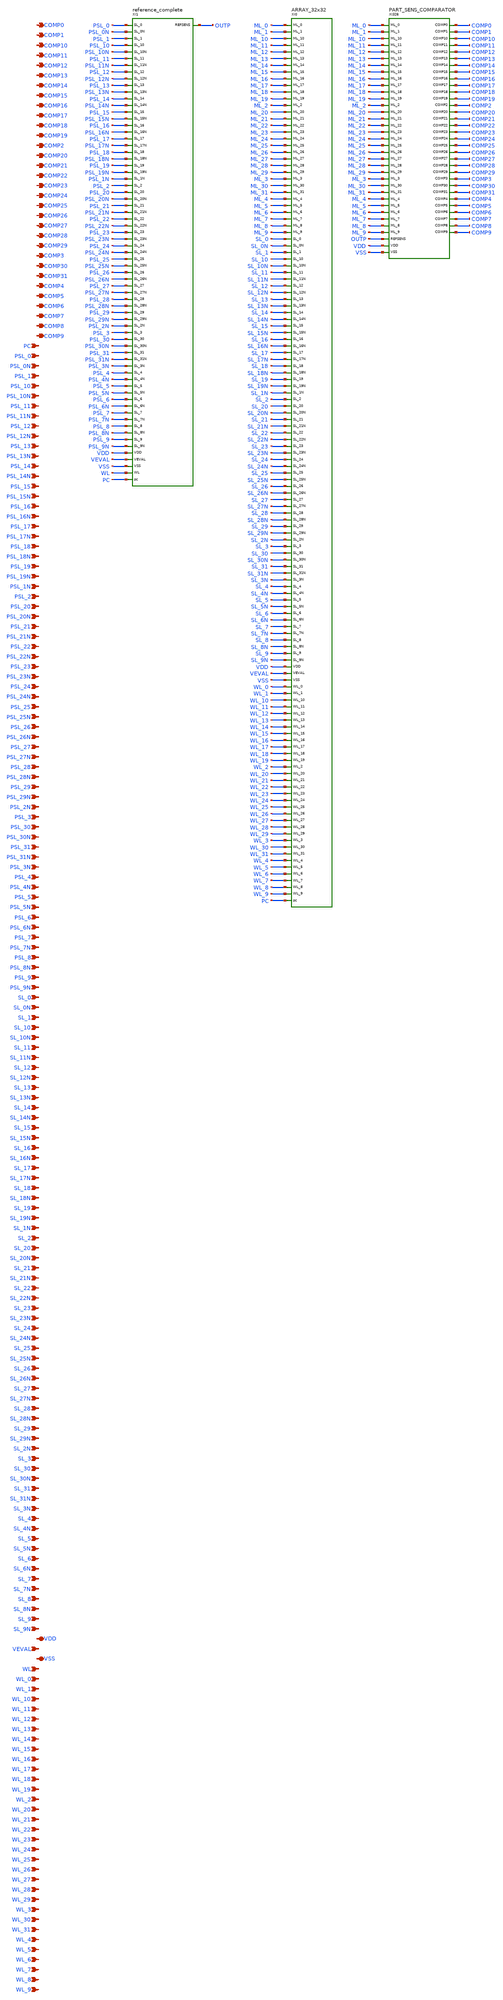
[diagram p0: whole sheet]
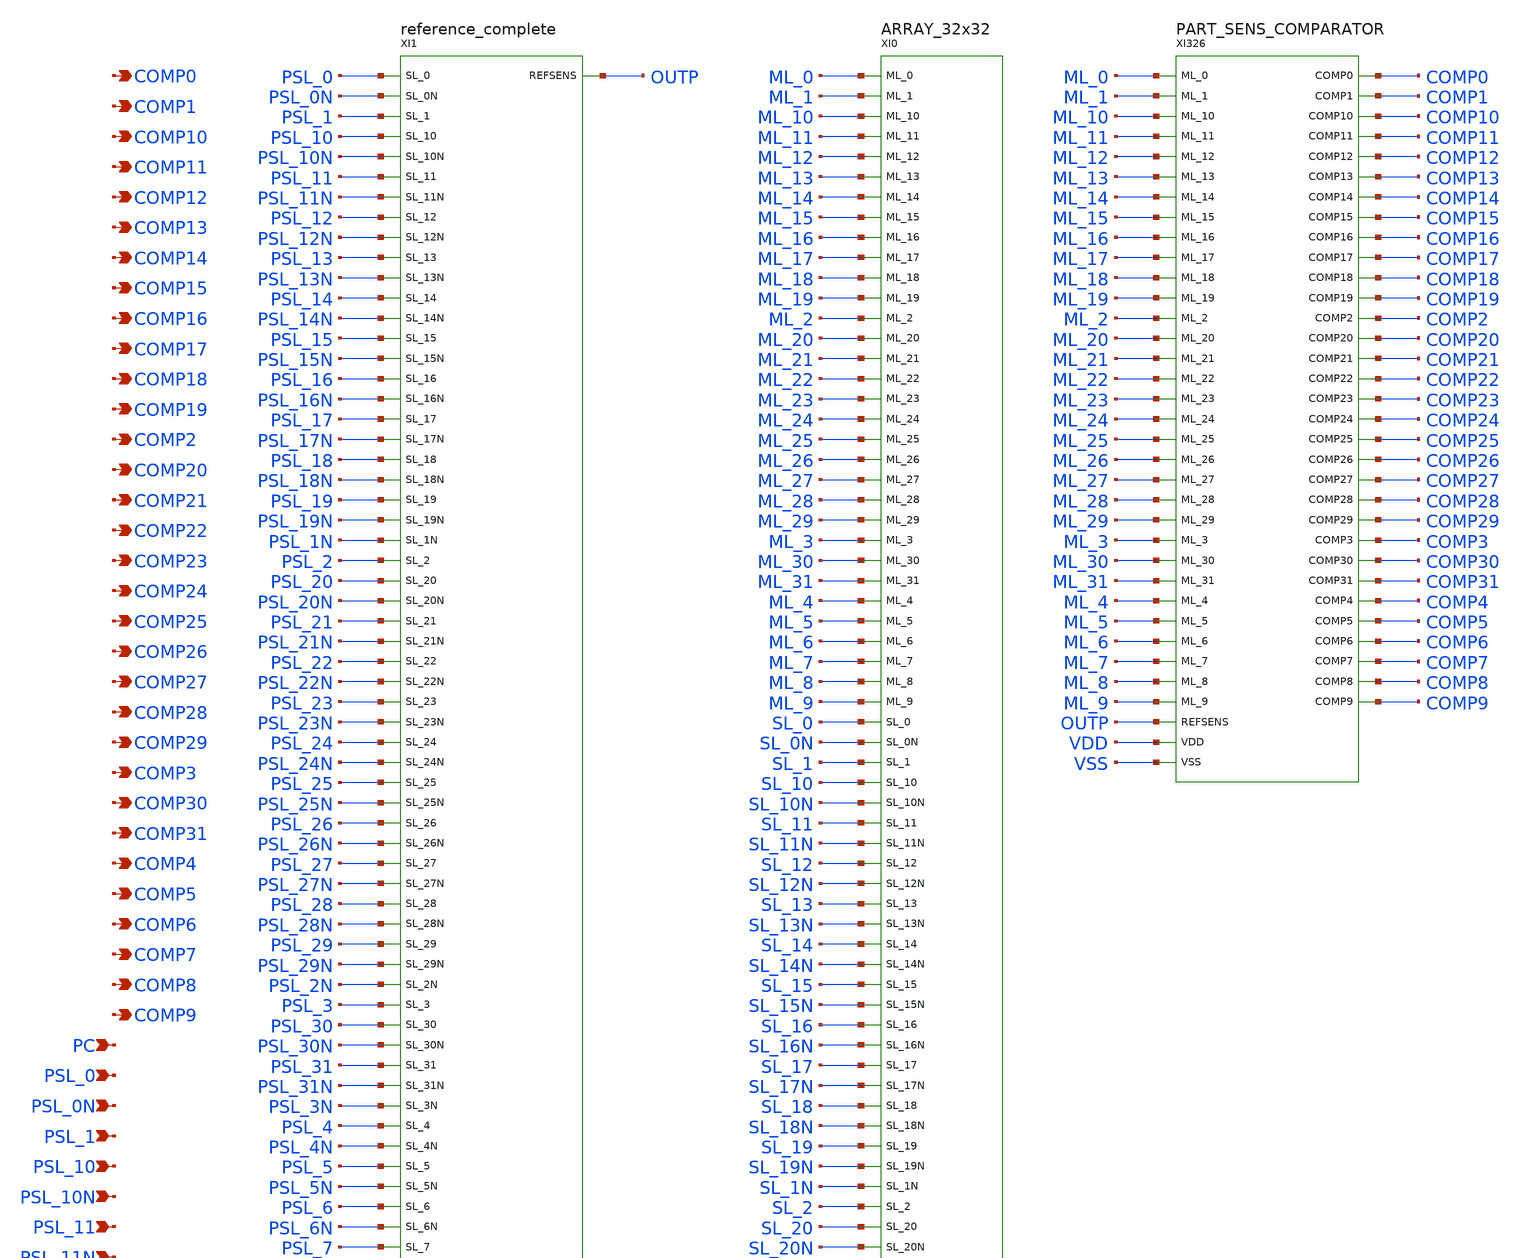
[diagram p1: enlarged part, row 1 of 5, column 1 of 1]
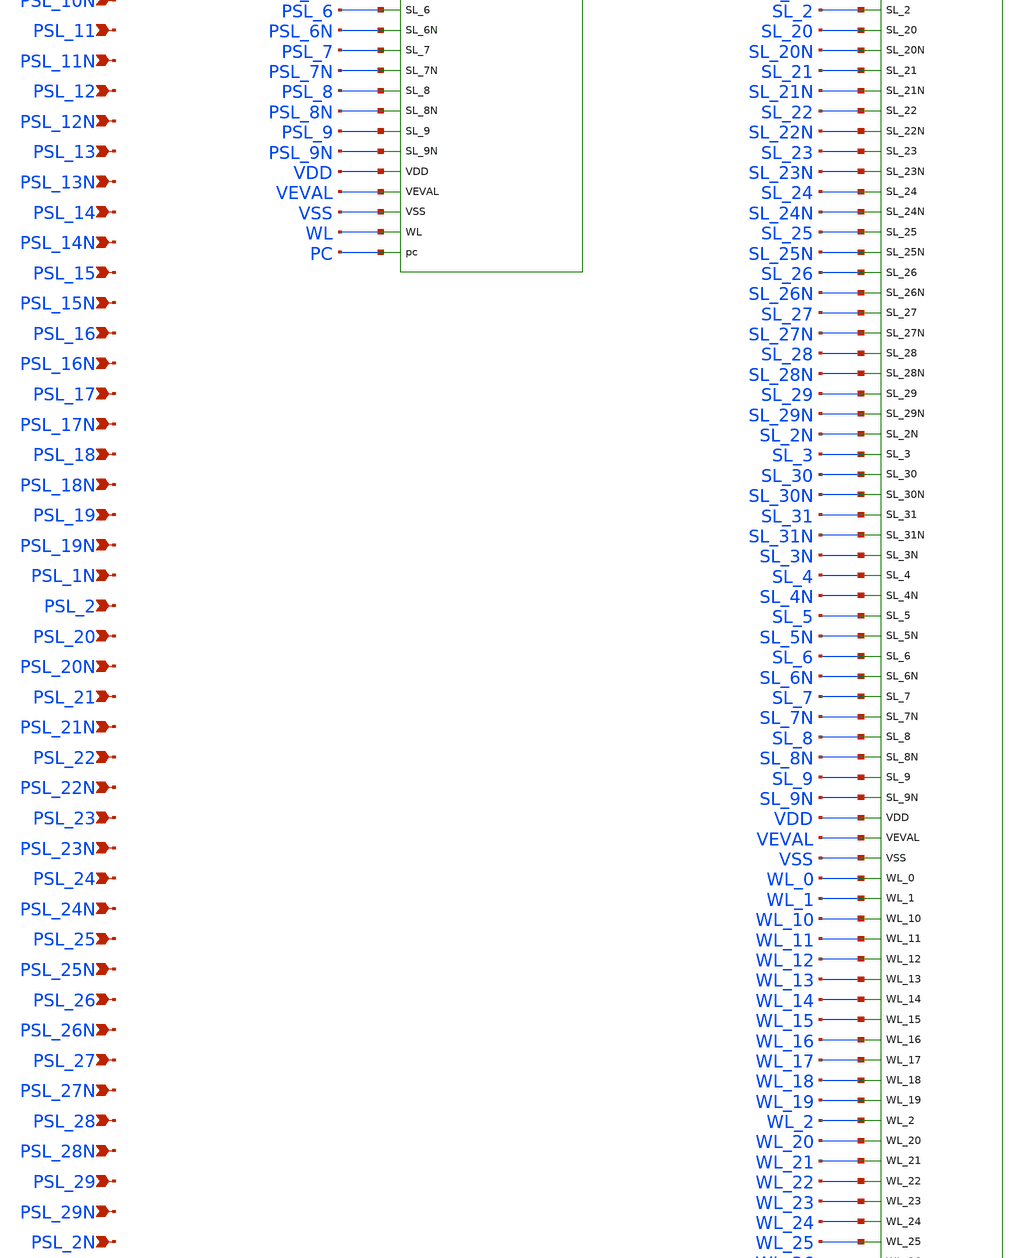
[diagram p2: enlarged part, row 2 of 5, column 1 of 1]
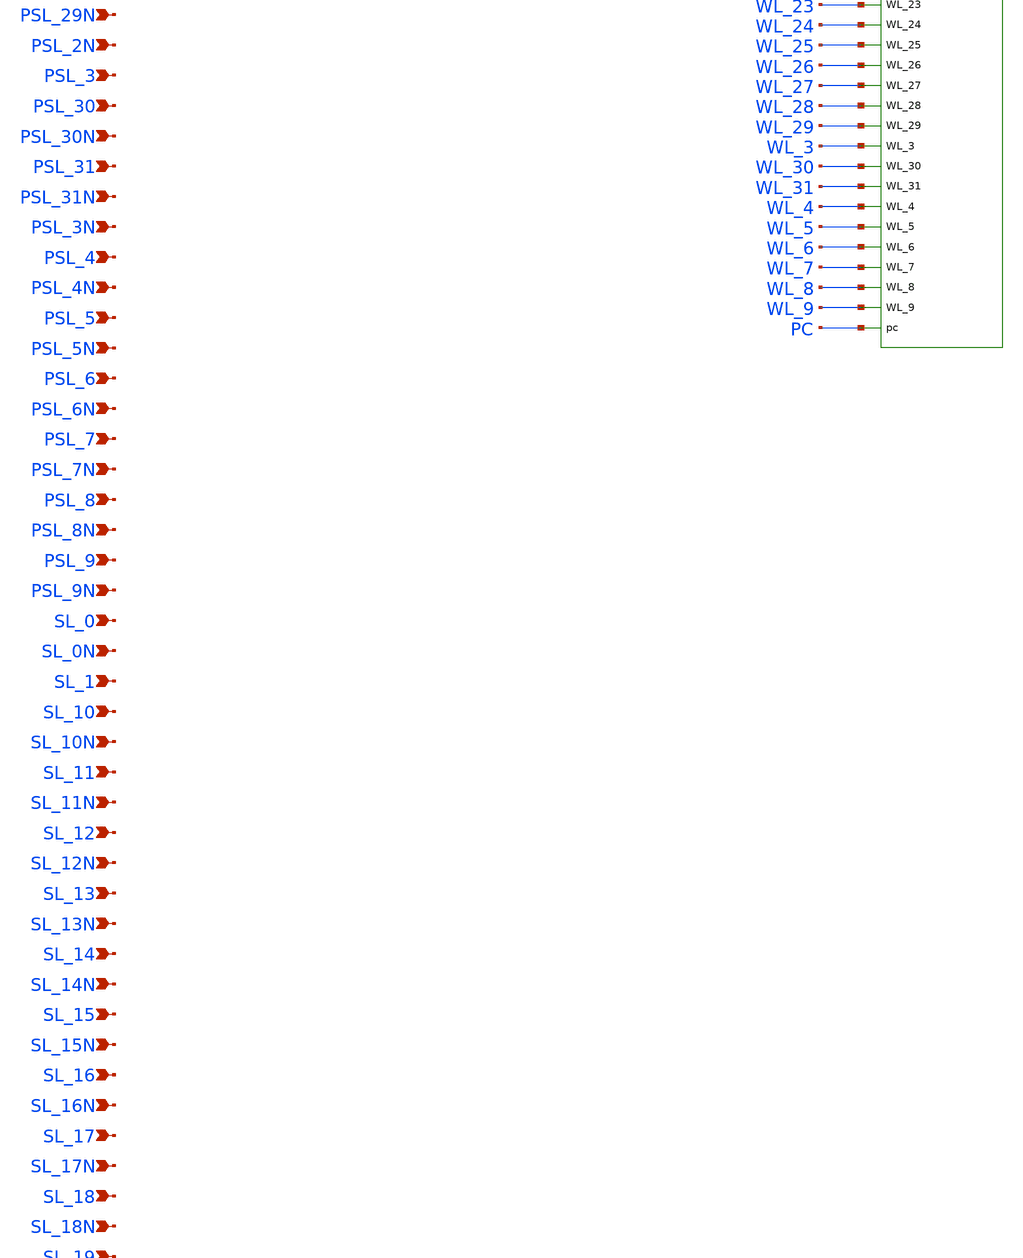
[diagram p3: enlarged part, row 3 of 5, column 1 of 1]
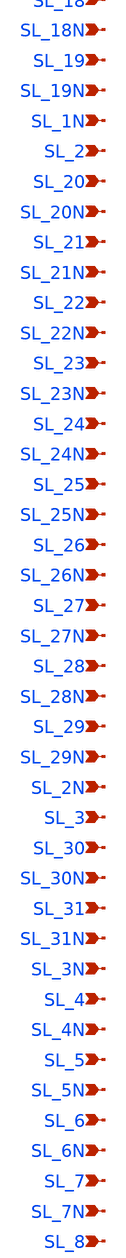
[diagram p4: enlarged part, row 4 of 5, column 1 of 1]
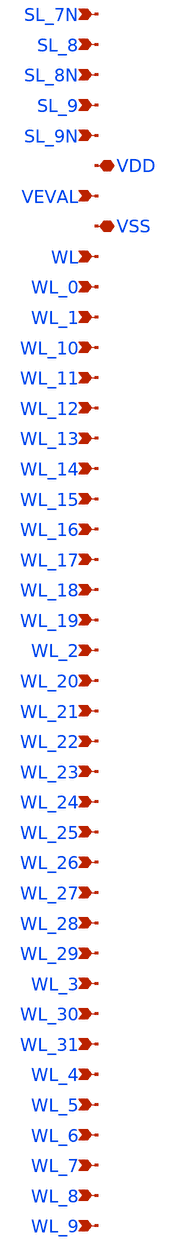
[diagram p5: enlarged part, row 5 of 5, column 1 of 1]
** sch_path: SoC6169-main/schematic/xschem/ANALOG_FIGURE.sch
* Copyright 2026 USFQ CAM team
* Licensed under the Apache License, Version 2.0 (the "License");
* you may not use this file except in compliance with the License.
* You may obtain a copy of the License at
* https://www.apache.org/licenses/LICENSE-2.0
* Unless required by applicable law or agreed to in writing, software
* distributed under the License is distributed on an "AS IS" BASIS,
* WITHOUT WARRANTIES OR CONDITIONS OF ANY KIND, either express or implied.
* See the License for the specific language governing permissions and
* limitations under the License.
**.subckt ANALOG_FIGURE COMP0 COMP1 COMP10 COMP11 COMP12 COMP13 COMP14 COMP15 COMP16 COMP17 COMP18
*+ COMP19 COMP2 COMP20 COMP21 COMP22 COMP23 COMP24 COMP25 COMP26 COMP27 COMP28 COMP29 COMP3 COMP30 COMP31
*+ COMP4 COMP5 COMP6 COMP7 COMP8 COMP9 PC PSL_0 PSL_0N PSL_1 PSL_10 PSL_10N PSL_11 PSL_11N PSL_12 PSL_12N
*+ PSL_13 PSL_13N PSL_14 PSL_14N PSL_15 PSL_15N PSL_16 PSL_16N PSL_17 PSL_17N PSL_18 PSL_18N PSL_19 PSL_19N
*+ PSL_1N PSL_2 PSL_20 PSL_20N PSL_21 PSL_21N PSL_22 PSL_22N PSL_23 PSL_23N PSL_24 PSL_24N PSL_25 PSL_25N
*+ PSL_26 PSL_26N PSL_27 PSL_27N PSL_28 PSL_28N PSL_29 PSL_29N PSL_2N PSL_3 PSL_30 PSL_30N PSL_31 PSL_31N
*+ PSL_3N PSL_4 PSL_4N PSL_5 PSL_5N PSL_6 PSL_6N PSL_7 PSL_7N PSL_8 PSL_8N PSL_9 PSL_9N SL_0 SL_0N SL_1 SL_10
*+ SL_10N SL_11 SL_11N SL_12 SL_12N SL_13 SL_13N SL_14 SL_14N SL_15 SL_15N SL_16 SL_16N SL_17 SL_17N SL_18
*+ SL_18N SL_19 SL_19N SL_1N SL_2 SL_20 SL_20N SL_21 SL_21N SL_22 SL_22N SL_23 SL_23N SL_24 SL_24N SL_25
*+ SL_25N SL_26 SL_26N SL_27 SL_27N SL_28 SL_28N SL_29 SL_29N SL_2N SL_3 SL_30 SL_30N SL_31 SL_31N SL_3N SL_4
*+ SL_4N SL_5 SL_5N SL_6 SL_6N SL_7 SL_7N SL_8 SL_8N SL_9 SL_9N VDD VEVAL VSS WL WL_0 WL_1 WL_10 WL_11 WL_12
*+ WL_13 WL_14 WL_15 WL_16 WL_17 WL_18 WL_19 WL_2 WL_20 WL_21 WL_22 WL_23 WL_24 WL_25 WL_26 WL_27 WL_28
*+ WL_29 WL_3 WL_30 WL_31 WL_4 WL_5 WL_6 WL_7 WL_8 WL_9
*.opin COMP0
*.opin COMP1
*.opin COMP10
*.opin COMP11
*.opin COMP12
*.opin COMP13
*.opin COMP14
*.opin COMP15
*.opin COMP16
*.opin COMP17
*.opin COMP18
*.opin COMP19
*.opin COMP2
*.opin COMP20
*.opin COMP21
*.opin COMP22
*.opin COMP23
*.opin COMP24
*.opin COMP25
*.opin COMP26
*.opin COMP27
*.opin COMP28
*.opin COMP29
*.opin COMP3
*.opin COMP30
*.opin COMP31
*.opin COMP4
*.opin COMP5
*.opin COMP6
*.opin COMP7
*.opin COMP8
*.opin COMP9
*.ipin PC
*.ipin PSL_0
*.ipin PSL_0N
*.ipin PSL_1
*.ipin PSL_10
*.ipin PSL_10N
*.ipin PSL_11
*.ipin PSL_11N
*.ipin PSL_12
*.ipin PSL_12N
*.ipin PSL_13
*.ipin PSL_13N
*.ipin PSL_14
*.ipin PSL_14N
*.ipin PSL_15
*.ipin PSL_15N
*.ipin PSL_16
*.ipin PSL_16N
*.ipin PSL_17
*.ipin PSL_17N
*.ipin PSL_18
*.ipin PSL_18N
*.ipin PSL_19
*.ipin PSL_19N
*.ipin PSL_1N
*.ipin PSL_2
*.ipin PSL_20
*.ipin PSL_20N
*.ipin PSL_21
*.ipin PSL_21N
*.ipin PSL_22
*.ipin PSL_22N
*.ipin PSL_23
*.ipin PSL_23N
*.ipin PSL_24
*.ipin PSL_24N
*.ipin PSL_25
*.ipin PSL_25N
*.ipin PSL_26
*.ipin PSL_26N
*.ipin PSL_27
*.ipin PSL_27N
*.ipin PSL_28
*.ipin PSL_28N
*.ipin PSL_29
*.ipin PSL_29N
*.ipin PSL_2N
*.ipin PSL_3
*.ipin PSL_30
*.ipin PSL_30N
*.ipin PSL_31
*.ipin PSL_31N
*.ipin PSL_3N
*.ipin PSL_4
*.ipin PSL_4N
*.ipin PSL_5
*.ipin PSL_5N
*.ipin PSL_6
*.ipin PSL_6N
*.ipin PSL_7
*.ipin PSL_7N
*.ipin PSL_8
*.ipin PSL_8N
*.ipin PSL_9
*.ipin PSL_9N
*.ipin SL_0
*.ipin SL_0N
*.ipin SL_1
*.ipin SL_10
*.ipin SL_10N
*.ipin SL_11
*.ipin SL_11N
*.ipin SL_12
*.ipin SL_12N
*.ipin SL_13
*.ipin SL_13N
*.ipin SL_14
*.ipin SL_14N
*.ipin SL_15
*.ipin SL_15N
*.ipin SL_16
*.ipin SL_16N
*.ipin SL_17
*.ipin SL_17N
*.ipin SL_18
*.ipin SL_18N
*.ipin SL_19
*.ipin SL_19N
*.ipin SL_1N
*.ipin SL_2
*.ipin SL_20
*.ipin SL_20N
*.ipin SL_21
*.ipin SL_21N
*.ipin SL_22
*.ipin SL_22N
*.ipin SL_23
*.ipin SL_23N
*.ipin SL_24
*.ipin SL_24N
*.ipin SL_25
*.ipin SL_25N
*.ipin SL_26
*.ipin SL_26N
*.ipin SL_27
*.ipin SL_27N
*.ipin SL_28
*.ipin SL_28N
*.ipin SL_29
*.ipin SL_29N
*.ipin SL_2N
*.ipin SL_3
*.ipin SL_30
*.ipin SL_30N
*.ipin SL_31
*.ipin SL_31N
*.ipin SL_3N
*.ipin SL_4
*.ipin SL_4N
*.ipin SL_5
*.ipin SL_5N
*.ipin SL_6
*.ipin SL_6N
*.ipin SL_7
*.ipin SL_7N
*.ipin SL_8
*.ipin SL_8N
*.ipin SL_9
*.ipin SL_9N
*.iopin VDD
*.ipin VEVAL
*.iopin VSS
*.ipin WL
*.ipin WL_0
*.ipin WL_1
*.ipin WL_10
*.ipin WL_11
*.ipin WL_12
*.ipin WL_13
*.ipin WL_14
*.ipin WL_15
*.ipin WL_16
*.ipin WL_17
*.ipin WL_18
*.ipin WL_19
*.ipin WL_2
*.ipin WL_20
*.ipin WL_21
*.ipin WL_22
*.ipin WL_23
*.ipin WL_24
*.ipin WL_25
*.ipin WL_26
*.ipin WL_27
*.ipin WL_28
*.ipin WL_29
*.ipin WL_3
*.ipin WL_30
*.ipin WL_31
*.ipin WL_4
*.ipin WL_5
*.ipin WL_6
*.ipin WL_7
*.ipin WL_8
*.ipin WL_9
XI1 OUTP PSL_0 PSL_0N PSL_1 PSL_10 PSL_10N PSL_11 PSL_11N PSL_12 PSL_12N PSL_13 PSL_13N PSL_14
+ PSL_14N PSL_15 PSL_15N PSL_16 PSL_16N PSL_17 PSL_17N PSL_18 PSL_18N PSL_19 PSL_19N PSL_1N PSL_2 PSL_20
+ PSL_20N PSL_21 PSL_21N PSL_22 PSL_22N PSL_23 PSL_23N PSL_24 PSL_24N PSL_25 PSL_25N PSL_26 PSL_26N PSL_27
+ PSL_27N PSL_28 PSL_28N PSL_29 PSL_29N PSL_2N PSL_3 PSL_30 PSL_30N PSL_31 PSL_31N PSL_3N PSL_4 PSL_4N PSL_5
+ PSL_5N PSL_6 PSL_6N PSL_7 PSL_7N PSL_8 PSL_8N PSL_9 PSL_9N VDD VEVAL VSS WL PC reference_complete
XI0 ML_0 ML_1 ML_10 ML_11 ML_12 ML_13 ML_14 ML_15 ML_16 ML_17 ML_18 ML_19 ML_2 ML_20 ML_21 ML_22
+ ML_23 ML_24 ML_25 ML_26 ML_27 ML_28 ML_29 ML_3 ML_30 ML_31 ML_4 ML_5 ML_6 ML_7 ML_8 ML_9 SL_0 SL_0N SL_1
+ SL_10 SL_10N SL_11 SL_11N SL_12 SL_12N SL_13 SL_13N SL_14 SL_14N SL_15 SL_15N SL_16 SL_16N SL_17 SL_17N
+ SL_18 SL_18N SL_19 SL_19N SL_1N SL_2 SL_20 SL_20N SL_21 SL_21N SL_22 SL_22N SL_23 SL_23N SL_24 SL_24N
+ SL_25 SL_25N SL_26 SL_26N SL_27 SL_27N SL_28 SL_28N SL_29 SL_29N SL_2N SL_3 SL_30 SL_30N SL_31 SL_31N
+ SL_3N SL_4 SL_4N SL_5 SL_5N SL_6 SL_6N SL_7 SL_7N SL_8 SL_8N SL_9 SL_9N VDD VEVAL VSS WL_0 WL_1 WL_10
+ WL_11 WL_12 WL_13 WL_14 WL_15 WL_16 WL_17 WL_18 WL_19 WL_2 WL_20 WL_21 WL_22 WL_23 WL_24 WL_25 WL_26
+ WL_27 WL_28 WL_29 WL_3 WL_30 WL_31 WL_4 WL_5 WL_6 WL_7 WL_8 WL_9 PC ARRAY_32x32
XI326 COMP0 COMP1 COMP10 COMP11 COMP12 COMP13 COMP14 COMP15 COMP16 COMP17 COMP18 COMP19 COMP2 COMP20
+ COMP21 COMP22 COMP23 COMP24 COMP25 COMP26 COMP27 COMP28 COMP29 COMP3 COMP30 COMP31 COMP4 COMP5 COMP6 COMP7
+ COMP8 COMP9 ML_0 ML_1 ML_10 ML_11 ML_12 ML_13 ML_14 ML_15 ML_16 ML_17 ML_18 ML_19 ML_2 ML_20 ML_21 ML_22
+ ML_23 ML_24 ML_25 ML_26 ML_27 ML_28 ML_29 ML_3 ML_30 ML_31 ML_4 ML_5 ML_6 ML_7 ML_8 ML_9 OUTP VDD VSS
+ PART_SENS_COMPARATOR
**.ends

* expanding   symbol:  reference_complete.sym # of pins=70
** sym_path: SoC6169-main/schematic/xschem/reference_complete.sym
** sch_path: SoC6169-main/schematic/xschem/reference_complete.sch
.subckt reference_complete REFSENS SL_0 SL_0N SL_1 SL_10 SL_10N SL_11 SL_11N SL_12 SL_12N SL_13
+ SL_13N SL_14 SL_14N SL_15 SL_15N SL_16 SL_16N SL_17 SL_17N SL_18 SL_18N SL_19 SL_19N SL_1N SL_2 SL_20
+ SL_20N SL_21 SL_21N SL_22 SL_22N SL_23 SL_23N SL_24 SL_24N SL_25 SL_25N SL_26 SL_26N SL_27 SL_27N SL_28
+ SL_28N SL_29 SL_29N SL_2N SL_3 SL_30 SL_30N SL_31 SL_31N SL_3N SL_4 SL_4N SL_5 SL_5N SL_6 SL_6N SL_7 SL_7N
+ SL_8 SL_8N SL_9 SL_9N VDD VEVAL VSS WL pc
*.opin REFSENS
*.ipin SL_0
*.ipin SL_0N
*.ipin SL_1
*.ipin SL_10
*.ipin SL_10N
*.ipin SL_11
*.ipin SL_11N
*.ipin SL_12
*.ipin SL_12N
*.ipin SL_13
*.ipin SL_13N
*.ipin SL_14
*.ipin SL_14N
*.ipin SL_15
*.ipin SL_15N
*.ipin SL_16
*.ipin SL_16N
*.ipin SL_17
*.ipin SL_17N
*.ipin SL_18
*.ipin SL_18N
*.ipin SL_19
*.ipin SL_19N
*.ipin SL_1N
*.ipin SL_2
*.ipin SL_20
*.ipin SL_20N
*.ipin SL_21
*.ipin SL_21N
*.ipin SL_22
*.ipin SL_22N
*.ipin SL_23
*.ipin SL_23N
*.ipin SL_24
*.ipin SL_24N
*.ipin SL_25
*.ipin SL_25N
*.ipin SL_26
*.ipin SL_26N
*.ipin SL_27
*.ipin SL_27N
*.ipin SL_28
*.ipin SL_28N
*.ipin SL_29
*.ipin SL_29N
*.ipin SL_2N
*.ipin SL_3
*.ipin SL_30
*.ipin SL_30N
*.ipin SL_31
*.ipin SL_31N
*.ipin SL_3N
*.ipin SL_4
*.ipin SL_4N
*.ipin SL_5
*.ipin SL_5N
*.ipin SL_6
*.ipin SL_6N
*.ipin SL_7
*.ipin SL_7N
*.ipin SL_8
*.ipin SL_8N
*.ipin SL_9
*.ipin SL_9N
*.iopin VDD
*.ipin VEVAL
*.iopin VSS
*.ipin WL
*.ipin pc
XI311 REFSENS net1 VDD VSS BUFFER
XI323 VSS ML_ref VDD net1 INV
XI0 ML_ref SL_0 SL_0N SL_1 SL_10 SL_10N SL_11 SL_11N SL_12 SL_12N SL_13 SL_13N SL_14 SL_14N SL_15
+ SL_15N SL_16 SL_16N SL_17 SL_17N SL_18 SL_18N SL_19 SL_19N SL_1N SL_2 SL_20 SL_20N SL_21 SL_21N SL_22
+ SL_22N SL_23 SL_23N SL_24 SL_24N SL_25 SL_25N SL_26 SL_26N SL_27 SL_27N SL_28 SL_28N SL_29 SL_29N SL_2N
+ SL_3 SL_30 SL_30N SL_31 SL_31N SL_3N SL_4 SL_4N SL_5 SL_5N SL_6 SL_6N SL_7 SL_7N SL_8 SL_8N SL_9 SL_9N
+ VDD VEVAL VSS WL pc WORD_32bits
.ends


* expanding   symbol:  ARRAY_32x32.sym # of pins=132
** sym_path: SoC6169-main/schematic/xschem/ARRAY_32x32.sym
** sch_path: SoC6169-main/schematic/xschem/ARRAY_32x32.sch
.subckt ARRAY_32x32 ML_0 ML_1 ML_10 ML_11 ML_12 ML_13 ML_14 ML_15 ML_16 ML_17 ML_18 ML_19 ML_2 ML_20
+ ML_21 ML_22 ML_23 ML_24 ML_25 ML_26 ML_27 ML_28 ML_29 ML_3 ML_30 ML_31 ML_4 ML_5 ML_6 ML_7 ML_8 ML_9 SL_0
+ SL_0N SL_1 SL_10 SL_10N SL_11 SL_11N SL_12 SL_12N SL_13 SL_13N SL_14 SL_14N SL_15 SL_15N SL_16 SL_16N
+ SL_17 SL_17N SL_18 SL_18N SL_19 SL_19N SL_1N SL_2 SL_20 SL_20N SL_21 SL_21N SL_22 SL_22N SL_23 SL_23N
+ SL_24 SL_24N SL_25 SL_25N SL_26 SL_26N SL_27 SL_27N SL_28 SL_28N SL_29 SL_29N SL_2N SL_3 SL_30 SL_30N
+ SL_31 SL_31N SL_3N SL_4 SL_4N SL_5 SL_5N SL_6 SL_6N SL_7 SL_7N SL_8 SL_8N SL_9 SL_9N VDD VEVAL VSS WL_0
+ WL_1 WL_10 WL_11 WL_12 WL_13 WL_14 WL_15 WL_16 WL_17 WL_18 WL_19 WL_2 WL_20 WL_21 WL_22 WL_23 WL_24
+ WL_25 WL_26 WL_27 WL_28 WL_29 WL_3 WL_30 WL_31 WL_4 WL_5 WL_6 WL_7 WL_8 WL_9 pc
*.iopin ML_0
*.iopin ML_1
*.iopin ML_10
*.iopin ML_11
*.iopin ML_12
*.iopin ML_13
*.iopin ML_14
*.iopin ML_15
*.iopin ML_16
*.iopin ML_17
*.iopin ML_18
*.iopin ML_19
*.iopin ML_2
*.iopin ML_20
*.iopin ML_21
*.iopin ML_22
*.iopin ML_23
*.iopin ML_24
*.iopin ML_25
*.iopin ML_26
*.iopin ML_27
*.iopin ML_28
*.iopin ML_29
*.iopin ML_3
*.iopin ML_30
*.iopin ML_31
*.iopin ML_4
*.iopin ML_5
*.iopin ML_6
*.iopin ML_7
*.iopin ML_8
*.iopin ML_9
*.ipin SL_0
*.ipin SL_0N
*.ipin SL_1
*.ipin SL_10
*.ipin SL_10N
*.ipin SL_11
*.ipin SL_11N
*.ipin SL_12
*.ipin SL_12N
*.ipin SL_13
*.ipin SL_13N
*.ipin SL_14
*.ipin SL_14N
*.ipin SL_15
*.ipin SL_15N
*.ipin SL_16
*.ipin SL_16N
*.ipin SL_17
*.ipin SL_17N
*.ipin SL_18
*.ipin SL_18N
*.ipin SL_19
*.ipin SL_19N
*.ipin SL_1N
*.ipin SL_2
*.ipin SL_20
*.ipin SL_20N
*.ipin SL_21
*.ipin SL_21N
*.ipin SL_22
*.ipin SL_22N
*.ipin SL_23
*.ipin SL_23N
*.ipin SL_24
*.ipin SL_24N
*.ipin SL_25
*.ipin SL_25N
*.ipin SL_26
*.ipin SL_26N
*.ipin SL_27
*.ipin SL_27N
*.ipin SL_28
*.ipin SL_28N
*.ipin SL_29
*.ipin SL_29N
*.ipin SL_2N
*.ipin SL_3
*.ipin SL_30
*.ipin SL_30N
*.ipin SL_31
*.ipin SL_31N
*.ipin SL_3N
*.ipin SL_4
*.ipin SL_4N
*.ipin SL_5
*.ipin SL_5N
*.ipin SL_6
*.ipin SL_6N
*.ipin SL_7
*.ipin SL_7N
*.ipin SL_8
*.ipin SL_8N
*.ipin SL_9
*.ipin SL_9N
*.iopin VDD
*.ipin VEVAL
*.iopin VSS
*.ipin WL_0
*.ipin WL_1
*.ipin WL_10
*.ipin WL_11
*.ipin WL_12
*.ipin WL_13
*.ipin WL_14
*.ipin WL_15
*.ipin WL_16
*.ipin WL_17
*.ipin WL_18
*.ipin WL_19
*.ipin WL_2
*.ipin WL_20
*.ipin WL_21
*.ipin WL_22
*.ipin WL_23
*.ipin WL_24
*.ipin WL_25
*.ipin WL_26
*.ipin WL_27
*.ipin WL_28
*.ipin WL_29
*.ipin WL_3
*.ipin WL_30
*.ipin WL_31
*.ipin WL_4
*.ipin WL_5
*.ipin WL_6
*.ipin WL_7
*.ipin WL_8
*.ipin WL_9
*.ipin pc
XI25 ML_14 SL_0 SL_0N SL_1 SL_10 SL_10N SL_11 SL_11N SL_12 SL_12N SL_13 SL_13N SL_14 SL_14N SL_15
+ SL_15N SL_16 SL_16N SL_17 SL_17N SL_18 SL_18N SL_19 SL_19N SL_1N SL_2 SL_20 SL_20N SL_21 SL_21N SL_22
+ SL_22N SL_23 SL_23N SL_24 SL_24N SL_25 SL_25N SL_26 SL_26N SL_27 SL_27N SL_28 SL_28N SL_29 SL_29N SL_2N
+ SL_3 SL_30 SL_30N SL_31 SL_31N SL_3N SL_4 SL_4N SL_5 SL_5N SL_6 SL_6N SL_7 SL_7N SL_8 SL_8N SL_9 SL_9N
+ VDD VEVAL VSS WL_14 pc WORD_32bits
XI24 ML_13 SL_0 SL_0N SL_1 SL_10 SL_10N SL_11 SL_11N SL_12 SL_12N SL_13 SL_13N SL_14 SL_14N SL_15
+ SL_15N SL_16 SL_16N SL_17 SL_17N SL_18 SL_18N SL_19 SL_19N SL_1N SL_2 SL_20 SL_20N SL_21 SL_21N SL_22
+ SL_22N SL_23 SL_23N SL_24 SL_24N SL_25 SL_25N SL_26 SL_26N SL_27 SL_27N SL_28 SL_28N SL_29 SL_29N SL_2N
+ SL_3 SL_30 SL_30N SL_31 SL_31N SL_3N SL_4 SL_4N SL_5 SL_5N SL_6 SL_6N SL_7 SL_7N SL_8 SL_8N SL_9 SL_9N
+ VDD VEVAL VSS WL_13 pc WORD_32bits
XI23 ML_12 SL_0 SL_0N SL_1 SL_10 SL_10N SL_11 SL_11N SL_12 SL_12N SL_13 SL_13N SL_14 SL_14N SL_15
+ SL_15N SL_16 SL_16N SL_17 SL_17N SL_18 SL_18N SL_19 SL_19N SL_1N SL_2 SL_20 SL_20N SL_21 SL_21N SL_22
+ SL_22N SL_23 SL_23N SL_24 SL_24N SL_25 SL_25N SL_26 SL_26N SL_27 SL_27N SL_28 SL_28N SL_29 SL_29N SL_2N
+ SL_3 SL_30 SL_30N SL_31 SL_31N SL_3N SL_4 SL_4N SL_5 SL_5N SL_6 SL_6N SL_7 SL_7N SL_8 SL_8N SL_9 SL_9N
+ VDD VEVAL VSS WL_12 pc WORD_32bits
XI47 ML_17 SL_0 SL_0N SL_1 SL_10 SL_10N SL_11 SL_11N SL_12 SL_12N SL_13 SL_13N SL_14 SL_14N SL_15
+ SL_15N SL_16 SL_16N SL_17 SL_17N SL_18 SL_18N SL_19 SL_19N SL_1N SL_2 SL_20 SL_20N SL_21 SL_21N SL_22
+ SL_22N SL_23 SL_23N SL_24 SL_24N SL_25 SL_25N SL_26 SL_26N SL_27 SL_27N SL_28 SL_28N SL_29 SL_29N SL_2N
+ SL_3 SL_30 SL_30N SL_31 SL_31N SL_3N SL_4 SL_4N SL_5 SL_5N SL_6 SL_6N SL_7 SL_7N SL_8 SL_8N SL_9 SL_9N
+ VDD VEVAL VSS WL_17 pc WORD_32bits
XI43 ML_18 SL_0 SL_0N SL_1 SL_10 SL_10N SL_11 SL_11N SL_12 SL_12N SL_13 SL_13N SL_14 SL_14N SL_15
+ SL_15N SL_16 SL_16N SL_17 SL_17N SL_18 SL_18N SL_19 SL_19N SL_1N SL_2 SL_20 SL_20N SL_21 SL_21N SL_22
+ SL_22N SL_23 SL_23N SL_24 SL_24N SL_25 SL_25N SL_26 SL_26N SL_27 SL_27N SL_28 SL_28N SL_29 SL_29N SL_2N
+ SL_3 SL_30 SL_30N SL_31 SL_31N SL_3N SL_4 SL_4N SL_5 SL_5N SL_6 SL_6N SL_7 SL_7N SL_8 SL_8N SL_9 SL_9N
+ VDD VEVAL VSS WL_18 pc WORD_32bits
XI49 ML_16 SL_0 SL_0N SL_1 SL_10 SL_10N SL_11 SL_11N SL_12 SL_12N SL_13 SL_13N SL_14 SL_14N SL_15
+ SL_15N SL_16 SL_16N SL_17 SL_17N SL_18 SL_18N SL_19 SL_19N SL_1N SL_2 SL_20 SL_20N SL_21 SL_21N SL_22
+ SL_22N SL_23 SL_23N SL_24 SL_24N SL_25 SL_25N SL_26 SL_26N SL_27 SL_27N SL_28 SL_28N SL_29 SL_29N SL_2N
+ SL_3 SL_30 SL_30N SL_31 SL_31N SL_3N SL_4 SL_4N SL_5 SL_5N SL_6 SL_6N SL_7 SL_7N SL_8 SL_8N SL_9 SL_9N
+ VDD VEVAL VSS WL_16 pc WORD_32bits
XI46 ML_22 SL_0 SL_0N SL_1 SL_10 SL_10N SL_11 SL_11N SL_12 SL_12N SL_13 SL_13N SL_14 SL_14N SL_15
+ SL_15N SL_16 SL_16N SL_17 SL_17N SL_18 SL_18N SL_19 SL_19N SL_1N SL_2 SL_20 SL_20N SL_21 SL_21N SL_22
+ SL_22N SL_23 SL_23N SL_24 SL_24N SL_25 SL_25N SL_26 SL_26N SL_27 SL_27N SL_28 SL_28N SL_29 SL_29N SL_2N
+ SL_3 SL_30 SL_30N SL_31 SL_31N SL_3N SL_4 SL_4N SL_5 SL_5N SL_6 SL_6N SL_7 SL_7N SL_8 SL_8N SL_9 SL_9N
+ VDD VEVAL VSS WL_22 pc WORD_32bits
XI48 ML_21 SL_0 SL_0N SL_1 SL_10 SL_10N SL_11 SL_11N SL_12 SL_12N SL_13 SL_13N SL_14 SL_14N SL_15
+ SL_15N SL_16 SL_16N SL_17 SL_17N SL_18 SL_18N SL_19 SL_19N SL_1N SL_2 SL_20 SL_20N SL_21 SL_21N SL_22
+ SL_22N SL_23 SL_23N SL_24 SL_24N SL_25 SL_25N SL_26 SL_26N SL_27 SL_27N SL_28 SL_28N SL_29 SL_29N SL_2N
+ SL_3 SL_30 SL_30N SL_31 SL_31N SL_3N SL_4 SL_4N SL_5 SL_5N SL_6 SL_6N SL_7 SL_7N SL_8 SL_8N SL_9 SL_9N
+ VDD VEVAL VSS WL_21 pc WORD_32bits
XI44 ML_19 SL_0 SL_0N SL_1 SL_10 SL_10N SL_11 SL_11N SL_12 SL_12N SL_13 SL_13N SL_14 SL_14N SL_15
+ SL_15N SL_16 SL_16N SL_17 SL_17N SL_18 SL_18N SL_19 SL_19N SL_1N SL_2 SL_20 SL_20N SL_21 SL_21N SL_22
+ SL_22N SL_23 SL_23N SL_24 SL_24N SL_25 SL_25N SL_26 SL_26N SL_27 SL_27N SL_28 SL_28N SL_29 SL_29N SL_2N
+ SL_3 SL_30 SL_30N SL_31 SL_31N SL_3N SL_4 SL_4N SL_5 SL_5N SL_6 SL_6N SL_7 SL_7N SL_8 SL_8N SL_9 SL_9N
+ VDD VEVAL VSS WL_19 pc WORD_32bits
XI45 ML_23 SL_0 SL_0N SL_1 SL_10 SL_10N SL_11 SL_11N SL_12 SL_12N SL_13 SL_13N SL_14 SL_14N SL_15
+ SL_15N SL_16 SL_16N SL_17 SL_17N SL_18 SL_18N SL_19 SL_19N SL_1N SL_2 SL_20 SL_20N SL_21 SL_21N SL_22
+ SL_22N SL_23 SL_23N SL_24 SL_24N SL_25 SL_25N SL_26 SL_26N SL_27 SL_27N SL_28 SL_28N SL_29 SL_29N SL_2N
+ SL_3 SL_30 SL_30N SL_31 SL_31N SL_3N SL_4 SL_4N SL_5 SL_5N SL_6 SL_6N SL_7 SL_7N SL_8 SL_8N SL_9 SL_9N
+ VDD VEVAL VSS WL_23 pc WORD_32bits
XI50 ML_20 SL_0 SL_0N SL_1 SL_10 SL_10N SL_11 SL_11N SL_12 SL_12N SL_13 SL_13N SL_14 SL_14N SL_15
+ SL_15N SL_16 SL_16N SL_17 SL_17N SL_18 SL_18N SL_19 SL_19N SL_1N SL_2 SL_20 SL_20N SL_21 SL_21N SL_22
+ SL_22N SL_23 SL_23N SL_24 SL_24N SL_25 SL_25N SL_26 SL_26N SL_27 SL_27N SL_28 SL_28N SL_29 SL_29N SL_2N
+ SL_3 SL_30 SL_30N SL_31 SL_31N SL_3N SL_4 SL_4N SL_5 SL_5N SL_6 SL_6N SL_7 SL_7N SL_8 SL_8N SL_9 SL_9N
+ VDD VEVAL VSS WL_20 pc WORD_32bits
XI22 ML_9 SL_0 SL_0N SL_1 SL_10 SL_10N SL_11 SL_11N SL_12 SL_12N SL_13 SL_13N SL_14 SL_14N SL_15
+ SL_15N SL_16 SL_16N SL_17 SL_17N SL_18 SL_18N SL_19 SL_19N SL_1N SL_2 SL_20 SL_20N SL_21 SL_21N SL_22
+ SL_22N SL_23 SL_23N SL_24 SL_24N SL_25 SL_25N SL_26 SL_26N SL_27 SL_27N SL_28 SL_28N SL_29 SL_29N SL_2N
+ SL_3 SL_30 SL_30N SL_31 SL_31N SL_3N SL_4 SL_4N SL_5 SL_5N SL_6 SL_6N SL_7 SL_7N SL_8 SL_8N SL_9 SL_9N
+ VDD VEVAL VSS WL_9 pc WORD_32bits
XI20 ML_10 SL_0 SL_0N SL_1 SL_10 SL_10N SL_11 SL_11N SL_12 SL_12N SL_13 SL_13N SL_14 SL_14N SL_15
+ SL_15N SL_16 SL_16N SL_17 SL_17N SL_18 SL_18N SL_19 SL_19N SL_1N SL_2 SL_20 SL_20N SL_21 SL_21N SL_22
+ SL_22N SL_23 SL_23N SL_24 SL_24N SL_25 SL_25N SL_26 SL_26N SL_27 SL_27N SL_28 SL_28N SL_29 SL_29N SL_2N
+ SL_3 SL_30 SL_30N SL_31 SL_31N SL_3N SL_4 SL_4N SL_5 SL_5N SL_6 SL_6N SL_7 SL_7N SL_8 SL_8N SL_9 SL_9N
+ VDD VEVAL VSS WL_10 pc WORD_32bits
XI10 ML_0 SL_0 SL_0N SL_1 SL_10 SL_10N SL_11 SL_11N SL_12 SL_12N SL_13 SL_13N SL_14 SL_14N SL_15
+ SL_15N SL_16 SL_16N SL_17 SL_17N SL_18 SL_18N SL_19 SL_19N SL_1N SL_2 SL_20 SL_20N SL_21 SL_21N SL_22
+ SL_22N SL_23 SL_23N SL_24 SL_24N SL_25 SL_25N SL_26 SL_26N SL_27 SL_27N SL_28 SL_28N SL_29 SL_29N SL_2N
+ SL_3 SL_30 SL_30N SL_31 SL_31N SL_3N SL_4 SL_4N SL_5 SL_5N SL_6 SL_6N SL_7 SL_7N SL_8 SL_8N SL_9 SL_9N
+ VDD VEVAL VSS WL_0 pc WORD_32bits
XI14 ML_4 SL_0 SL_0N SL_1 SL_10 SL_10N SL_11 SL_11N SL_12 SL_12N SL_13 SL_13N SL_14 SL_14N SL_15
+ SL_15N SL_16 SL_16N SL_17 SL_17N SL_18 SL_18N SL_19 SL_19N SL_1N SL_2 SL_20 SL_20N SL_21 SL_21N SL_22
+ SL_22N SL_23 SL_23N SL_24 SL_24N SL_25 SL_25N SL_26 SL_26N SL_27 SL_27N SL_28 SL_28N SL_29 SL_29N SL_2N
+ SL_3 SL_30 SL_30N SL_31 SL_31N SL_3N SL_4 SL_4N SL_5 SL_5N SL_6 SL_6N SL_7 SL_7N SL_8 SL_8N SL_9 SL_9N
+ VDD VEVAL VSS WL_4 pc WORD_32bits
XI15 ML_5 SL_0 SL_0N SL_1 SL_10 SL_10N SL_11 SL_11N SL_12 SL_12N SL_13 SL_13N SL_14 SL_14N SL_15
+ SL_15N SL_16 SL_16N SL_17 SL_17N SL_18 SL_18N SL_19 SL_19N SL_1N SL_2 SL_20 SL_20N SL_21 SL_21N SL_22
+ SL_22N SL_23 SL_23N SL_24 SL_24N SL_25 SL_25N SL_26 SL_26N SL_27 SL_27N SL_28 SL_28N SL_29 SL_29N SL_2N
+ SL_3 SL_30 SL_30N SL_31 SL_31N SL_3N SL_4 SL_4N SL_5 SL_5N SL_6 SL_6N SL_7 SL_7N SL_8 SL_8N SL_9 SL_9N
+ VDD VEVAL VSS WL_5 pc WORD_32bits
XI17 ML_7 SL_0 SL_0N SL_1 SL_10 SL_10N SL_11 SL_11N SL_12 SL_12N SL_13 SL_13N SL_14 SL_14N SL_15
+ SL_15N SL_16 SL_16N SL_17 SL_17N SL_18 SL_18N SL_19 SL_19N SL_1N SL_2 SL_20 SL_20N SL_21 SL_21N SL_22
+ SL_22N SL_23 SL_23N SL_24 SL_24N SL_25 SL_25N SL_26 SL_26N SL_27 SL_27N SL_28 SL_28N SL_29 SL_29N SL_2N
+ SL_3 SL_30 SL_30N SL_31 SL_31N SL_3N SL_4 SL_4N SL_5 SL_5N SL_6 SL_6N SL_7 SL_7N SL_8 SL_8N SL_9 SL_9N
+ VDD VEVAL VSS WL_7 pc WORD_32bits
XI16 ML_6 SL_0 SL_0N SL_1 SL_10 SL_10N SL_11 SL_11N SL_12 SL_12N SL_13 SL_13N SL_14 SL_14N SL_15
+ SL_15N SL_16 SL_16N SL_17 SL_17N SL_18 SL_18N SL_19 SL_19N SL_1N SL_2 SL_20 SL_20N SL_21 SL_21N SL_22
+ SL_22N SL_23 SL_23N SL_24 SL_24N SL_25 SL_25N SL_26 SL_26N SL_27 SL_27N SL_28 SL_28N SL_29 SL_29N SL_2N
+ SL_3 SL_30 SL_30N SL_31 SL_31N SL_3N SL_4 SL_4N SL_5 SL_5N SL_6 SL_6N SL_7 SL_7N SL_8 SL_8N SL_9 SL_9N
+ VDD VEVAL VSS WL_6 pc WORD_32bits
XI13 ML_3 SL_0 SL_0N SL_1 SL_10 SL_10N SL_11 SL_11N SL_12 SL_12N SL_13 SL_13N SL_14 SL_14N SL_15
+ SL_15N SL_16 SL_16N SL_17 SL_17N SL_18 SL_18N SL_19 SL_19N SL_1N SL_2 SL_20 SL_20N SL_21 SL_21N SL_22
+ SL_22N SL_23 SL_23N SL_24 SL_24N SL_25 SL_25N SL_26 SL_26N SL_27 SL_27N SL_28 SL_28N SL_29 SL_29N SL_2N
+ SL_3 SL_30 SL_30N SL_31 SL_31N SL_3N SL_4 SL_4N SL_5 SL_5N SL_6 SL_6N SL_7 SL_7N SL_8 SL_8N SL_9 SL_9N
+ VDD VEVAL VSS WL_3 pc WORD_32bits
XI18 ML_15 SL_0 SL_0N SL_1 SL_10 SL_10N SL_11 SL_11N SL_12 SL_12N SL_13 SL_13N SL_14 SL_14N SL_15
+ SL_15N SL_16 SL_16N SL_17 SL_17N SL_18 SL_18N SL_19 SL_19N SL_1N SL_2 SL_20 SL_20N SL_21 SL_21N SL_22
+ SL_22N SL_23 SL_23N SL_24 SL_24N SL_25 SL_25N SL_26 SL_26N SL_27 SL_27N SL_28 SL_28N SL_29 SL_29N SL_2N
+ SL_3 SL_30 SL_30N SL_31 SL_31N SL_3N SL_4 SL_4N SL_5 SL_5N SL_6 SL_6N SL_7 SL_7N SL_8 SL_8N SL_9 SL_9N
+ VDD VEVAL VSS WL_15 pc WORD_32bits
XI51 ML_28 SL_0 SL_0N SL_1 SL_10 SL_10N SL_11 SL_11N SL_12 SL_12N SL_13 SL_13N SL_14 SL_14N SL_15
+ SL_15N SL_16 SL_16N SL_17 SL_17N SL_18 SL_18N SL_19 SL_19N SL_1N SL_2 SL_20 SL_20N SL_21 SL_21N SL_22
+ SL_22N SL_23 SL_23N SL_24 SL_24N SL_25 SL_25N SL_26 SL_26N SL_27 SL_27N SL_28 SL_28N SL_29 SL_29N SL_2N
+ SL_3 SL_30 SL_30N SL_31 SL_31N SL_3N SL_4 SL_4N SL_5 SL_5N SL_6 SL_6N SL_7 SL_7N SL_8 SL_8N SL_9 SL_9N
+ VDD VEVAL VSS WL_28 pc WORD_32bits
XI57 ML_27 SL_0 SL_0N SL_1 SL_10 SL_10N SL_11 SL_11N SL_12 SL_12N SL_13 SL_13N SL_14 SL_14N SL_15
+ SL_15N SL_16 SL_16N SL_17 SL_17N SL_18 SL_18N SL_19 SL_19N SL_1N SL_2 SL_20 SL_20N SL_21 SL_21N SL_22
+ SL_22N SL_23 SL_23N SL_24 SL_24N SL_25 SL_25N SL_26 SL_26N SL_27 SL_27N SL_28 SL_28N SL_29 SL_29N SL_2N
+ SL_3 SL_30 SL_30N SL_31 SL_31N SL_3N SL_4 SL_4N SL_5 SL_5N SL_6 SL_6N SL_7 SL_7N SL_8 SL_8N SL_9 SL_9N
+ VDD VEVAL VSS WL_27 pc WORD_32bits
XI53 ML_29 SL_0 SL_0N SL_1 SL_10 SL_10N SL_11 SL_11N SL_12 SL_12N SL_13 SL_13N SL_14 SL_14N SL_15
+ SL_15N SL_16 SL_16N SL_17 SL_17N SL_18 SL_18N SL_19 SL_19N SL_1N SL_2 SL_20 SL_20N SL_21 SL_21N SL_22
+ SL_22N SL_23 SL_23N SL_24 SL_24N SL_25 SL_25N SL_26 SL_26N SL_27 SL_27N SL_28 SL_28N SL_29 SL_29N SL_2N
+ SL_3 SL_30 SL_30N SL_31 SL_31N SL_3N SL_4 SL_4N SL_5 SL_5N SL_6 SL_6N SL_7 SL_7N SL_8 SL_8N SL_9 SL_9N
+ VDD VEVAL VSS WL_29 pc WORD_32bits
XI54 ML_25 SL_0 SL_0N SL_1 SL_10 SL_10N SL_11 SL_11N SL_12 SL_12N SL_13 SL_13N SL_14 SL_14N SL_15
+ SL_15N SL_16 SL_16N SL_17 SL_17N SL_18 SL_18N SL_19 SL_19N SL_1N SL_2 SL_20 SL_20N SL_21 SL_21N SL_22
+ SL_22N SL_23 SL_23N SL_24 SL_24N SL_25 SL_25N SL_26 SL_26N SL_27 SL_27N SL_28 SL_28N SL_29 SL_29N SL_2N
+ SL_3 SL_30 SL_30N SL_31 SL_31N SL_3N SL_4 SL_4N SL_5 SL_5N SL_6 SL_6N SL_7 SL_7N SL_8 SL_8N SL_9 SL_9N
+ VDD VEVAL VSS WL_25 pc WORD_32bits
XI19 ML_11 SL_0 SL_0N SL_1 SL_10 SL_10N SL_11 SL_11N SL_12 SL_12N SL_13 SL_13N SL_14 SL_14N SL_15
+ SL_15N SL_16 SL_16N SL_17 SL_17N SL_18 SL_18N SL_19 SL_19N SL_1N SL_2 SL_20 SL_20N SL_21 SL_21N SL_22
+ SL_22N SL_23 SL_23N SL_24 SL_24N SL_25 SL_25N SL_26 SL_26N SL_27 SL_27N SL_28 SL_28N SL_29 SL_29N SL_2N
+ SL_3 SL_30 SL_30N SL_31 SL_31N SL_3N SL_4 SL_4N SL_5 SL_5N SL_6 SL_6N SL_7 SL_7N SL_8 SL_8N SL_9 SL_9N
+ VDD VEVAL VSS WL_11 pc WORD_32bits
XI52 ML_24 SL_0 SL_0N SL_1 SL_10 SL_10N SL_11 SL_11N SL_12 SL_12N SL_13 SL_13N SL_14 SL_14N SL_15
+ SL_15N SL_16 SL_16N SL_17 SL_17N SL_18 SL_18N SL_19 SL_19N SL_1N SL_2 SL_20 SL_20N SL_21 SL_21N SL_22
+ SL_22N SL_23 SL_23N SL_24 SL_24N SL_25 SL_25N SL_26 SL_26N SL_27 SL_27N SL_28 SL_28N SL_29 SL_29N SL_2N
+ SL_3 SL_30 SL_30N SL_31 SL_31N SL_3N SL_4 SL_4N SL_5 SL_5N SL_6 SL_6N SL_7 SL_7N SL_8 SL_8N SL_9 SL_9N
+ VDD VEVAL VSS WL_24 pc WORD_32bits
XI26 ML_8 SL_0 SL_0N SL_1 SL_10 SL_10N SL_11 SL_11N SL_12 SL_12N SL_13 SL_13N SL_14 SL_14N SL_15
+ SL_15N SL_16 SL_16N SL_17 SL_17N SL_18 SL_18N SL_19 SL_19N SL_1N SL_2 SL_20 SL_20N SL_21 SL_21N SL_22
+ SL_22N SL_23 SL_23N SL_24 SL_24N SL_25 SL_25N SL_26 SL_26N SL_27 SL_27N SL_28 SL_28N SL_29 SL_29N SL_2N
+ SL_3 SL_30 SL_30N SL_31 SL_31N SL_3N SL_4 SL_4N SL_5 SL_5N SL_6 SL_6N SL_7 SL_7N SL_8 SL_8N SL_9 SL_9N
+ VDD VEVAL VSS WL_8 pc WORD_32bits
XI58 ML_26 SL_0 SL_0N SL_1 SL_10 SL_10N SL_11 SL_11N SL_12 SL_12N SL_13 SL_13N SL_14 SL_14N SL_15
+ SL_15N SL_16 SL_16N SL_17 SL_17N SL_18 SL_18N SL_19 SL_19N SL_1N SL_2 SL_20 SL_20N SL_21 SL_21N SL_22
+ SL_22N SL_23 SL_23N SL_24 SL_24N SL_25 SL_25N SL_26 SL_26N SL_27 SL_27N SL_28 SL_28N SL_29 SL_29N SL_2N
+ SL_3 SL_30 SL_30N SL_31 SL_31N SL_3N SL_4 SL_4N SL_5 SL_5N SL_6 SL_6N SL_7 SL_7N SL_8 SL_8N SL_9 SL_9N
+ VDD VEVAL VSS WL_26 pc WORD_32bits
XI56 ML_31 SL_0 SL_0N SL_1 SL_10 SL_10N SL_11 SL_11N SL_12 SL_12N SL_13 SL_13N SL_14 SL_14N SL_15
+ SL_15N SL_16 SL_16N SL_17 SL_17N SL_18 SL_18N SL_19 SL_19N SL_1N SL_2 SL_20 SL_20N SL_21 SL_21N SL_22
+ SL_22N SL_23 SL_23N SL_24 SL_24N SL_25 SL_25N SL_26 SL_26N SL_27 SL_27N SL_28 SL_28N SL_29 SL_29N SL_2N
+ SL_3 SL_30 SL_30N SL_31 SL_31N SL_3N SL_4 SL_4N SL_5 SL_5N SL_6 SL_6N SL_7 SL_7N SL_8 SL_8N SL_9 SL_9N
+ VDD VEVAL VSS WL_31 pc WORD_32bits
XI55 ML_30 SL_0 SL_0N SL_1 SL_10 SL_10N SL_11 SL_11N SL_12 SL_12N SL_13 SL_13N SL_14 SL_14N SL_15
+ SL_15N SL_16 SL_16N SL_17 SL_17N SL_18 SL_18N SL_19 SL_19N SL_1N SL_2 SL_20 SL_20N SL_21 SL_21N SL_22
+ SL_22N SL_23 SL_23N SL_24 SL_24N SL_25 SL_25N SL_26 SL_26N SL_27 SL_27N SL_28 SL_28N SL_29 SL_29N SL_2N
+ SL_3 SL_30 SL_30N SL_31 SL_31N SL_3N SL_4 SL_4N SL_5 SL_5N SL_6 SL_6N SL_7 SL_7N SL_8 SL_8N SL_9 SL_9N
+ VDD VEVAL VSS WL_30 pc WORD_32bits
XI11 ML_1 SL_0 SL_0N SL_1 SL_10 SL_10N SL_11 SL_11N SL_12 SL_12N SL_13 SL_13N SL_14 SL_14N SL_15
+ SL_15N SL_16 SL_16N SL_17 SL_17N SL_18 SL_18N SL_19 SL_19N SL_1N SL_2 SL_20 SL_20N SL_21 SL_21N SL_22
+ SL_22N SL_23 SL_23N SL_24 SL_24N SL_25 SL_25N SL_26 SL_26N SL_27 SL_27N SL_28 SL_28N SL_29 SL_29N SL_2N
+ SL_3 SL_30 SL_30N SL_31 SL_31N SL_3N SL_4 SL_4N SL_5 SL_5N SL_6 SL_6N SL_7 SL_7N SL_8 SL_8N SL_9 SL_9N
+ VDD VEVAL VSS WL_1 pc WORD_32bits
XI12 ML_2 SL_0 SL_0N SL_1 SL_10 SL_10N SL_11 SL_11N SL_12 SL_12N SL_13 SL_13N SL_14 SL_14N SL_15
+ SL_15N SL_16 SL_16N SL_17 SL_17N SL_18 SL_18N SL_19 SL_19N SL_1N SL_2 SL_20 SL_20N SL_21 SL_21N SL_22
+ SL_22N SL_23 SL_23N SL_24 SL_24N SL_25 SL_25N SL_26 SL_26N SL_27 SL_27N SL_28 SL_28N SL_29 SL_29N SL_2N
+ SL_3 SL_30 SL_30N SL_31 SL_31N SL_3N SL_4 SL_4N SL_5 SL_5N SL_6 SL_6N SL_7 SL_7N SL_8 SL_8N SL_9 SL_9N
+ VDD VEVAL VSS WL_2 pc WORD_32bits
.ends


* expanding   symbol:  PART_SENS_COMPARATOR.sym # of pins=67
** sym_path: SoC6169-main/schematic/xschem/PART_SENS_COMPARATOR.sym
** sch_path: SoC6169-main/schematic/xschem/PART_SENS_COMPARATOR.sch
.subckt PART_SENS_COMPARATOR COMP0 COMP1 COMP10 COMP11 COMP12 COMP13 COMP14 COMP15 COMP16 COMP17
+ COMP18 COMP19 COMP2 COMP20 COMP21 COMP22 COMP23 COMP24 COMP25 COMP26 COMP27 COMP28 COMP29 COMP3 COMP30
+ COMP31 COMP4 COMP5 COMP6 COMP7 COMP8 COMP9 ML_0 ML_1 ML_10 ML_11 ML_12 ML_13 ML_14 ML_15 ML_16 ML_17 ML_18
+ ML_19 ML_2 ML_20 ML_21 ML_22 ML_23 ML_24 ML_25 ML_26 ML_27 ML_28 ML_29 ML_3 ML_30 ML_31 ML_4 ML_5 ML_6
+ ML_7 ML_8 ML_9 REFSENS VDD VSS
*.opin COMP0
*.opin COMP1
*.opin COMP10
*.opin COMP11
*.opin COMP12
*.opin COMP13
*.opin COMP14
*.opin COMP15
*.opin COMP16
*.opin COMP17
*.opin COMP18
*.opin COMP19
*.opin COMP2
*.opin COMP20
*.opin COMP21
*.opin COMP22
*.opin COMP23
*.opin COMP24
*.opin COMP25
*.opin COMP26
*.opin COMP27
*.opin COMP28
*.opin COMP29
*.opin COMP3
*.opin COMP30
*.opin COMP31
*.opin COMP4
*.opin COMP5
*.opin COMP6
*.opin COMP7
*.opin COMP8
*.opin COMP9
*.ipin ML_0
*.ipin ML_1
*.ipin ML_10
*.ipin ML_11
*.ipin ML_12
*.ipin ML_13
*.ipin ML_14
*.ipin ML_15
*.ipin ML_16
*.ipin ML_17
*.ipin ML_18
*.ipin ML_19
*.ipin ML_2
*.ipin ML_20
*.ipin ML_21
*.ipin ML_22
*.ipin ML_23
*.ipin ML_24
*.ipin ML_25
*.ipin ML_26
*.ipin ML_27
*.ipin ML_28
*.ipin ML_29
*.ipin ML_3
*.ipin ML_30
*.ipin ML_31
*.ipin ML_4
*.ipin ML_5
*.ipin ML_6
*.ipin ML_7
*.ipin ML_8
*.ipin ML_9
*.ipin REFSENS
*.iopin VDD
*.iopin VSS
XI3 VSS ML_0 ML_1 ML_10 ML_11 ML_12 ML_13 ML_14 ML_15 ML_16 ML_17 ML_18 ML_19 ML_2 ML_20 ML_21 ML_22
+ ML_23 ML_24 ML_25 ML_26 ML_27 ML_28 ML_29 ML_3 ML_30 ML_31 ML_4 ML_5 ML_6 ML_7 ML_8 ML_9 net32 net31
+ net22 net21 net20 net19 net18 net17 net16 net15 net14 net13 net30 net12 net11 net10 net9 net8 net7 net6
+ net5 net4 net3 net29 net2 net1 net28 net27 net26 net25 net24 net23 VDD inverter_sens
XI4 COMP0 COMP1 COMP10 COMP11 COMP12 COMP13 COMP14 COMP15 COMP16 COMP17 COMP18 COMP19 COMP2 COMP20
+ COMP21 COMP22 COMP23 COMP24 COMP25 COMP26 COMP27 COMP28 COMP29 COMP3 COMP30 COMP31 COMP4 COMP5 COMP6 COMP7
+ COMP8 COMP9 REFSENS net32 net31 net22 net21 net20 net19 net18 net17 net16 net15 net14 net13 net30 net12
+ net11 net10 net9 net8 net7 net6 net5 net4 net3 net29 net2 net1 net28 net27 net26 net25 net24 net23 VDD
+ VSS COMPARATOR_NEWBUFFER_64x32
.ends


* expanding   symbol:  BUFFER.sym # of pins=4
** sym_path: SoC6169-main/schematic/xschem/BUFFER.sym
** sch_path: SoC6169-main/schematic/xschem/BUFFER.sch
.subckt BUFFER OUTP OUTPRE VDD VSS
*.opin OUTP
*.ipin OUTPRE
*.iopin VDD
*.iopin VSS
XMN0 OUTP medio VSS VSS sg13_lv_nmos w=3u l=130n ng=1 m=1 mm_ok=1
XMP0 OUTP medio VDD VDD sg13_lv_pmos w=6u l=130n ng=1 m=1 mm_ok=1
XI306 VSS OUTPRE VDD medio INV
.ends


* expanding   symbol:  INV.sym # of pins=4
** sym_path: SoC6169-main/schematic/xschem/INV.sym
** sch_path: SoC6169-main/schematic/xschem/INV.sch
.subckt INV GND IN VDD Y
*.iopin GND
*.ipin IN
*.iopin VDD
*.opin Y
XMN0 Y IN GND GND sg13_lv_nmos w=200n l=130n ng=1 m=1 mm_ok=1
XMP0 Y IN VDD VDD sg13_lv_pmos w=400n l=130n ng=1 m=1 mm_ok=1
.ends


* expanding   symbol:  WORD_32bits.sym # of pins=70
** sym_path: SoC6169-main/schematic/xschem/WORD_32bits.sym
** sch_path: SoC6169-main/schematic/xschem/WORD_32bits.sch
.subckt WORD_32bits ML SL_0 SL_0N SL_1 SL_10 SL_10N SL_11 SL_11N SL_12 SL_12N SL_13 SL_13N SL_14
+ SL_14N SL_15 SL_15N SL_16 SL_16N SL_17 SL_17N SL_18 SL_18N SL_19 SL_19N SL_1N SL_2 SL_20 SL_20N SL_21
+ SL_21N SL_22 SL_22N SL_23 SL_23N SL_24 SL_24N SL_25 SL_25N SL_26 SL_26N SL_27 SL_27N SL_28 SL_28N SL_29
+ SL_29N SL_2N SL_3 SL_30 SL_30N SL_31 SL_31N SL_3N SL_4 SL_4N SL_5 SL_5N SL_6 SL_6N SL_7 SL_7N SL_8 SL_8N
+ SL_9 SL_9N VDD VEVAL VSS WL pc
*.iopin ML
*.ipin SL_0
*.ipin SL_0N
*.ipin SL_1
*.ipin SL_10
*.ipin SL_10N
*.ipin SL_11
*.ipin SL_11N
*.ipin SL_12
*.ipin SL_12N
*.ipin SL_13
*.ipin SL_13N
*.ipin SL_14
*.ipin SL_14N
*.ipin SL_15
*.ipin SL_15N
*.ipin SL_16
*.ipin SL_16N
*.ipin SL_17
*.ipin SL_17N
*.ipin SL_18
*.ipin SL_18N
*.ipin SL_19
*.ipin SL_19N
*.ipin SL_1N
*.ipin SL_2
*.ipin SL_20
*.ipin SL_20N
*.ipin SL_21
*.ipin SL_21N
*.ipin SL_22
*.ipin SL_22N
*.ipin SL_23
*.ipin SL_23N
*.ipin SL_24
*.ipin SL_24N
*.ipin SL_25
*.ipin SL_25N
*.ipin SL_26
*.ipin SL_26N
*.ipin SL_27
*.ipin SL_27N
*.ipin SL_28
*.ipin SL_28N
*.ipin SL_29
*.ipin SL_29N
*.ipin SL_2N
*.ipin SL_3
*.ipin SL_30
*.ipin SL_30N
*.ipin SL_31
*.ipin SL_31N
*.ipin SL_3N
*.ipin SL_4
*.ipin SL_4N
*.ipin SL_5
*.ipin SL_5N
*.ipin SL_6
*.ipin SL_6N
*.ipin SL_7
*.ipin SL_7N
*.ipin SL_8
*.ipin SL_8N
*.ipin SL_9
*.ipin SL_9N
*.iopin VDD
*.ipin VEVAL
*.iopin VSS
*.ipin WL
*.ipin pc
XI31 ML SL_27 SL_27N VDD VEVAL VSS WL CELL
XI30 ML SL_24 SL_24N VDD VEVAL VSS WL CELL
XI29 ML SL_25 SL_25N VDD VEVAL VSS WL CELL
XI28 ML SL_26 SL_26N VDD VEVAL VSS WL CELL
XI27 ML SL_28 SL_28N VDD VEVAL VSS WL CELL
XI26 ML SL_29 SL_29N VDD VEVAL VSS WL CELL
XI25 ML SL_30 SL_30N VDD VEVAL VSS WL CELL
XI24 ML SL_31 SL_31N VDD VEVAL VSS WL CELL
XI23 ML SL_19 SL_19N VDD VEVAL VSS WL CELL
XI22 ML SL_16 SL_16N VDD VEVAL VSS WL CELL
XI21 ML SL_17 SL_17N VDD VEVAL VSS WL CELL
XI20 ML SL_18 SL_18N VDD VEVAL VSS WL CELL
XI19 ML SL_20 SL_20N VDD VEVAL VSS WL CELL
XI18 ML SL_21 SL_21N VDD VEVAL VSS WL CELL
XI17 ML SL_22 SL_22N VDD VEVAL VSS WL CELL
XI15 ML SL_11 SL_11N VDD VEVAL VSS WL CELL
XI14 ML SL_8 SL_8N VDD VEVAL VSS WL CELL
XI13 ML SL_9 SL_9N VDD VEVAL VSS WL CELL
XI12 ML SL_10 SL_10N VDD VEVAL VSS WL CELL
XI10 ML SL_12 SL_12N VDD VEVAL VSS WL CELL
XI6 ML SL_13 SL_13N VDD VEVAL VSS WL CELL
XI2 ML SL_14 SL_14N VDD VEVAL VSS WL CELL
XI1 ML SL_15 SL_15N VDD VEVAL VSS WL CELL
XI11 ML SL_3 SL_3N VDD VEVAL VSS WL CELL
XI9 ML SL_0 SL_0N VDD VEVAL VSS WL CELL
XI8 ML SL_1 SL_1N VDD VEVAL VSS WL CELL
XI7 ML SL_2 SL_2N VDD VEVAL VSS WL CELL
XI5 ML SL_4 SL_4N VDD VEVAL VSS WL CELL
XI4 ML SL_5 SL_5N VDD VEVAL VSS WL CELL
XI3 ML SL_6 SL_6N VDD VEVAL VSS WL CELL
XI0 ML SL_7 SL_7N VDD VEVAL VSS WL CELL
XI16 ML SL_23 SL_23N VDD VEVAL VSS WL CELL
XMP0 ML pc VDD VDD sg13_lv_pmos w=2u l=130n ng=1 m=1 mm_ok=1
.ends


* expanding   symbol:  inverter_sens.sym # of pins=66
** sym_path: SoC6169-main/schematic/xschem/inverter_sens.sym
** sch_path: SoC6169-main/schematic/xschem/inverter_sens.sch
.subckt inverter_sens GND ML_0 ML_1 ML_10 ML_11 ML_12 ML_13 ML_14 ML_15 ML_16 ML_17 ML_18 ML_19 ML_2
+ ML_20 ML_21 ML_22 ML_23 ML_24 ML_25 ML_26 ML_27 ML_28 ML_29 ML_3 ML_30 ML_31 ML_4 ML_5 ML_6 ML_7 ML_8
+ ML_9 OUT0 OUT1 OUT10 OUT11 OUT12 OUT13 OUT14 OUT15 OUT16 OUT17 OUT18 OUT19 OUT2 OUT20 OUT21 OUT22 OUT23
+ OUT24 OUT25 OUT26 OUT27 OUT28 OUT29 OUT3 OUT30 OUT31 OUT4 OUT5 OUT6 OUT7 OUT8 OUT9 VDD
*.iopin GND
*.ipin ML_0
*.ipin ML_1
*.ipin ML_10
*.ipin ML_11
*.ipin ML_12
*.ipin ML_13
*.ipin ML_14
*.ipin ML_15
*.ipin ML_16
*.ipin ML_17
*.ipin ML_18
*.ipin ML_19
*.ipin ML_2
*.ipin ML_20
*.ipin ML_21
*.ipin ML_22
*.ipin ML_23
*.ipin ML_24
*.ipin ML_25
*.ipin ML_26
*.ipin ML_27
*.ipin ML_28
*.ipin ML_29
*.ipin ML_3
*.ipin ML_30
*.ipin ML_31
*.ipin ML_4
*.ipin ML_5
*.ipin ML_6
*.ipin ML_7
*.ipin ML_8
*.ipin ML_9
*.opin OUT0
*.opin OUT1
*.opin OUT10
*.opin OUT11
*.opin OUT12
*.opin OUT13
*.opin OUT14
*.opin OUT15
*.opin OUT16
*.opin OUT17
*.opin OUT18
*.opin OUT19
*.opin OUT2
*.opin OUT20
*.opin OUT21
*.opin OUT22
*.opin OUT23
*.opin OUT24
*.opin OUT25
*.opin OUT26
*.opin OUT27
*.opin OUT28
*.opin OUT29
*.opin OUT3
*.opin OUT30
*.opin OUT31
*.opin OUT4
*.opin OUT5
*.opin OUT6
*.opin OUT7
*.opin OUT8
*.opin OUT9
*.iopin VDD
XI33 GND ML_1 VDD OUT1 INV
XI32 GND ML_0 VDD OUT0 INV
XI60 GND ML_26 VDD OUT26 INV
XI58 GND ML_25 VDD OUT25 INV
XI38 GND ML_6 VDD OUT6 INV
XI59 GND ML_27 VDD OUT27 INV
XI41 GND ML_9 VDD OUT9 INV
XI35 GND ML_3 VDD OUT3 INV
XI51 GND ML_18 VDD OUT18 INV
XI50 GND ML_19 VDD OUT19 INV
XI49 GND ML_17 VDD OUT17 INV
XI44 GND ML_14 VDD OUT14 INV
XI46 GND ML_13 VDD OUT13 INV
XI48 GND ML_16 VDD OUT16 INV
XI47 GND ML_12 VDD OUT12 INV
XI34 GND ML_2 VDD OUT2 INV
XI55 GND ML_30 VDD OUT30 INV
XI57 GND ML_29 VDD OUT29 INV
XI56 GND ML_31 VDD OUT31 INV
XI37 GND ML_5 VDD OUT5 INV
XI40 GND ML_8 VDD OUT8 INV
XI43 GND ML_10 VDD OUT10 INV
XI52 GND ML_20 VDD OUT20 INV
XI54 GND ML_28 VDD OUT28 INV
XI53 GND ML_24 VDD OUT24 INV
XI61 GND ML_22 VDD OUT22 INV
XI36 GND ML_4 VDD OUT4 INV
XI63 GND ML_21 VDD OUT21 INV
XI62 GND ML_23 VDD OUT23 INV
XI39 GND ML_7 VDD OUT7 INV
XI42 GND ML_11 VDD OUT11 INV
XI45 GND ML_15 VDD OUT15 INV
.ends


* expanding   symbol:  COMPARATOR_NEWBUFFER_64x32.sym # of pins=67
** sym_path: SoC6169-main/schematic/xschem/COMPARATOR_NEWBUFFER_64x32.sym
** sch_path: SoC6169-main/schematic/xschem/COMPARATOR_NEWBUFFER_64x32.sch
.subckt COMPARATOR_NEWBUFFER_64x32 COMP0 COMP1 COMP10 COMP11 COMP12 COMP13 COMP14 COMP15 COMP16
+ COMP17 COMP18 COMP19 COMP2 COMP20 COMP21 COMP22 COMP23 COMP24 COMP25 COMP26 COMP27 COMP28 COMP29 COMP3
+ COMP30 COMP31 COMP4 COMP5 COMP6 COMP7 COMP8 COMP9 REFSENS SENSML0 SENSML1 SENSML10 SENSML11 SENSML12
+ SENSML13 SENSML14 SENSML15 SENSML16 SENSML17 SENSML18 SENSML19 SENSML2 SENSML20 SENSML21 SENSML22 SENSML23
+ SENSML24 SENSML25 SENSML26 SENSML27 SENSML28 SENSML29 SENSML3 SENSML30 SENSML31 SENSML4 SENSML5 SENSML6
+ SENSML7 SENSML8 SENSML9 VDD VSS
*.opin COMP0
*.opin COMP1
*.opin COMP10
*.opin COMP11
*.opin COMP12
*.opin COMP13
*.opin COMP14
*.opin COMP15
*.opin COMP16
*.opin COMP17
*.opin COMP18
*.opin COMP19
*.opin COMP2
*.opin COMP20
*.opin COMP21
*.opin COMP22
*.opin COMP23
*.opin COMP24
*.opin COMP25
*.opin COMP26
*.opin COMP27
*.opin COMP28
*.opin COMP29
*.opin COMP3
*.opin COMP30
*.opin COMP31
*.opin COMP4
*.opin COMP5
*.opin COMP6
*.opin COMP7
*.opin COMP8
*.opin COMP9
*.ipin REFSENS
*.ipin SENSML0
*.ipin SENSML1
*.ipin SENSML10
*.ipin SENSML11
*.ipin SENSML12
*.ipin SENSML13
*.ipin SENSML14
*.ipin SENSML15
*.ipin SENSML16
*.ipin SENSML17
*.ipin SENSML18
*.ipin SENSML19
*.ipin SENSML2
*.ipin SENSML20
*.ipin SENSML21
*.ipin SENSML22
*.ipin SENSML23
*.ipin SENSML24
*.ipin SENSML25
*.ipin SENSML26
*.ipin SENSML27
*.ipin SENSML28
*.ipin SENSML29
*.ipin SENSML3
*.ipin SENSML30
*.ipin SENSML31
*.ipin SENSML4
*.ipin SENSML5
*.ipin SENSML6
*.ipin SENSML7
*.ipin SENSML8
*.ipin SENSML9
*.iopin VDD
*.iopin VSS
XI36 REFSENS SENSML0 COMP0 net12 VDD VSS flip_flop
XI38 REFSENS SENSML2 COMP2 net11 VDD VSS flip_flop
XI37 REFSENS SENSML1 COMP1 net10 VDD VSS flip_flop
XI39 REFSENS SENSML3 COMP3 net9 VDD VSS flip_flop
XI40 REFSENS SENSML4 COMP4 net8 VDD VSS flip_flop
XI42 REFSENS SENSML6 COMP6 net7 VDD VSS flip_flop
XI41 REFSENS SENSML5 COMP5 net6 VDD VSS flip_flop
XI43 REFSENS SENSML7 COMP7 net5 VDD VSS flip_flop
XI44 REFSENS SENSML8 COMP8 net4 VDD VSS flip_flop
XI46 REFSENS SENSML10 COMP10 net3 VDD VSS flip_flop
XI45 REFSENS SENSML9 COMP9 net2 VDD VSS flip_flop
XI47 REFSENS SENSML11 COMP11 net1 VDD VSS flip_flop
XI48 REFSENS SENSML12 COMP12 net32 VDD VSS flip_flop
XI50 REFSENS SENSML14 COMP14 net31 VDD VSS flip_flop
XI49 REFSENS SENSML13 COMP13 net30 VDD VSS flip_flop
XI51 REFSENS SENSML15 COMP15 net29 VDD VSS flip_flop
XI52 REFSENS SENSML16 COMP16 net28 VDD VSS flip_flop
XI54 REFSENS SENSML19 COMP19 net27 VDD VSS flip_flop
XI53 REFSENS SENSML17 COMP17 net26 VDD VSS flip_flop
XI55 REFSENS SENSML18 COMP18 net25 VDD VSS flip_flop
XI56 REFSENS SENSML20 COMP20 net24 VDD VSS flip_flop
XI58 REFSENS SENSML22 COMP22 net23 VDD VSS flip_flop
XI57 REFSENS SENSML21 COMP21 net22 VDD VSS flip_flop
XI59 REFSENS SENSML23 COMP23 net21 VDD VSS flip_flop
XI60 REFSENS SENSML24 COMP24 net20 VDD VSS flip_flop
XI62 REFSENS SENSML26 COMP26 net19 VDD VSS flip_flop
XI61 REFSENS SENSML25 COMP25 net18 VDD VSS flip_flop
XI63 REFSENS SENSML27 COMP27 net17 VDD VSS flip_flop
XI64 REFSENS SENSML28 COMP28 net16 VDD VSS flip_flop
XI65 REFSENS SENSML29 COMP29 net15 VDD VSS flip_flop
XI66 REFSENS SENSML30 COMP30 net14 VDD VSS flip_flop
XI67 REFSENS SENSML31 COMP31 net13 VDD VSS flip_flop
.ends


* expanding   symbol:  CELL.sym # of pins=7
** sym_path: SoC6169-main/schematic/xschem/CELL.sym
** sch_path: SoC6169-main/schematic/xschem/CELL.sch
.subckt CELL ML SL SL_N VDD VEVAL VSS WL
*.iopin ML
*.ipin SL
*.ipin SL_N
*.iopin VDD
*.ipin VEVAL
*.iopin VSS
*.ipin WL
XI7 VSS net1 VDD net2 INV
XI4 VSS net2 VDD net1 INV
XMN5 net11 VEVAL VSS VSS sg13_lv_nmos w=350n l=130n ng=1 m=1 mm_ok=1
XMN4 net11 net3 ML VSS sg13_lv_nmos w=740n l=130n ng=1 m=1 mm_ok=1
XMN3 net3 net2 SL VSS sg13_lv_nmos w=740n l=130n ng=1 m=1 mm_ok=1
XMN2 net3 net1 SL_N VSS sg13_lv_nmos w=740n l=130n ng=1 m=1 mm_ok=1
XMN1 SL_N WL net1 VSS sg13_lv_nmos w=740n l=130n ng=1 m=1 mm_ok=1
XMN0 SL WL net2 VSS sg13_lv_nmos w=740n l=130n ng=1 m=1 mm_ok=1
.ends


* expanding   symbol:  flip_flop.sym # of pins=6
** sym_path: SoC6169-main/schematic/xschem/flip_flop.sym
** sch_path: SoC6169-main/schematic/xschem/flip_flop.sch
.subckt flip_flop CLK D Q Q_n VDD VSS
*.ipin CLK
*.ipin D
*.opin Q
*.opin Q_n
*.iopin VDD
*.iopin VSS
XI7 VSS Q_n VDD Q INV
XI5 VSS Q_n VDD net14 INV
XI4 VSS net17 VDD Q_n INV
XI3 VSS net9 VDD net15 INV
XI2 VSS CLK VDD net12 INV
XI1 VSS net8 VDD net9 INV
XI0 VSS D VDD net5 INV
XMN4 net17 net12 net14 VSS sg13_lv_nmos w=740n l=130n ng=1 m=1 mm_ok=1
XMN3 net9 CLK net17 VSS sg13_lv_nmos w=740n l=130n ng=1 m=1 mm_ok=1
XMN2 net8 CLK net15 VSS sg13_lv_nmos w=740n l=130n ng=1 m=1 mm_ok=1
XMN0 net5 net12 net8 VSS sg13_lv_nmos w=740n l=130n ng=1 m=1 mm_ok=1
XMP4 net17 CLK net14 VDD sg13_lv_pmos w=1120n l=130n ng=1 m=1 mm_ok=1
XMP3 net9 net12 net17 VDD sg13_lv_pmos w=1120n l=130n ng=1 m=1 mm_ok=1
XMP2 net8 net12 net15 VDD sg13_lv_pmos w=1120n l=130n ng=1 m=1 mm_ok=1
XMP0 net5 CLK net8 VDD sg13_lv_pmos w=1120n l=130n ng=1 m=1 mm_ok=1
.ends

.end
